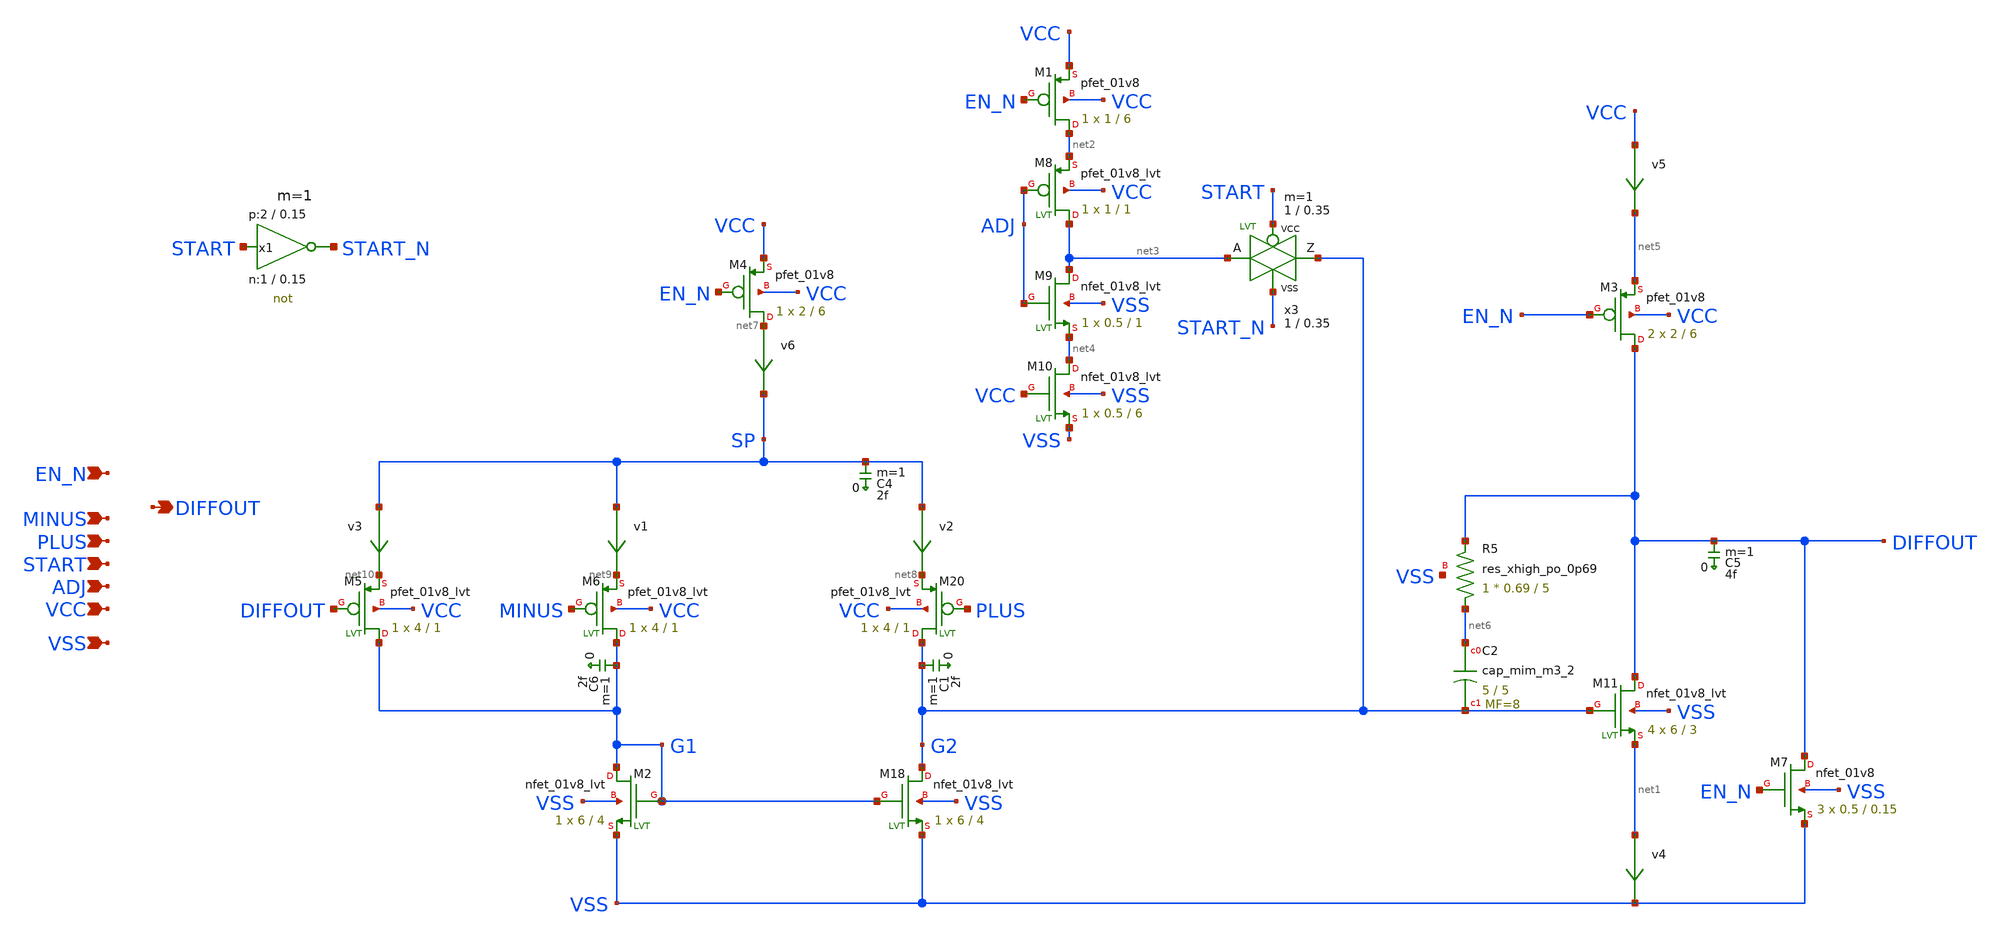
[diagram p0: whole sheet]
** sch_path: xyce/sky130A-xyce/libs.tech/xschem/sky130_tests/bandgap_opamp.sch
* Copyright 2020 Stefan Frederik Schippers
* Licensed under the Apache License, Version 2.0 (the "License");
* you may not use this file except in compliance with the License.
* You may obtain a copy of the License at
* https://www.apache.org/licenses/LICENSE-2.0
* Unless required by applicable law or agreed to in writing, software
* distributed under the License is distributed on an "AS IS" BASIS,
* WITHOUT WARRANTIES OR CONDITIONS OF ANY KIND, either express or implied.
* See the License for the specific language governing permissions and
* limitations under the License.
**.subckt bandgap_opamp PLUS MINUS EN_N VSS VCC DIFFOUT ADJ START
*.ipin PLUS
*.ipin MINUS
*.ipin EN_N
*.ipin VSS
*.ipin VCC
*.opin DIFFOUT
*.ipin ADJ
*.ipin START
C6 G1 0 2f m=1
XM4 net7 EN_N VCC VCC sky130_fd_pr__pfet_01v8 L=6 W=2 nf=1 ad='W * 0.29' as='W * 0.29' pd='W + 2 * 0.29'
+ ps='W + 2 * 0.29' nrd=0 nrs=0 sa=0 sb=0 sd=0 mult=1 m=1
XM18 G2 G1 VSS VSS sky130_fd_pr__nfet_01v8_lvt L=4 W=6 nf=1 ad='W * 0.29' as='W * 0.29' pd='2*(W + 0.29)'
+ ps='2*(W + 0.29)' nrd=0 nrs=0 sa=0 sb=0 sd=0 mult=1 m=1
XM2 G1 G1 VSS VSS sky130_fd_pr__nfet_01v8_lvt L=4 W=6 nf=1 ad='W * 0.29' as='W * 0.29' pd='2*(W + 0.29)'
+ ps='2*(W + 0.29)' nrd=0 nrs=0 sa=0 sb=0 sd=0 mult=1 m=1
XM20 G2 PLUS net8 VCC sky130_fd_pr__pfet_01v8_lvt L=1 W=4 nf=1 ad='W * 0.29' as='W * 0.29' pd='2*(W + 0.29)'
+ ps='2*(W + 0.29)' nrd=0 nrs=0 sa=0 sb=0 sd=0 mult=1 m=1
XM6 G1 MINUS net9 VCC sky130_fd_pr__pfet_01v8_lvt L=1 W=4 nf=1 ad='W * 0.29' as='W * 0.29' pd='2*(W + 0.29)'
+ ps='2*(W + 0.29)' nrd=0 nrs=0 sa=0 sb=0 sd=0 mult=1 m=1
v1 SP net9 0
.save i(v1)
C4 SP 0 2f m=1
C1 G2 0 2f m=1
C5 DIFFOUT 0 4f m=1
XM11 DIFFOUT G2 net1 VSS sky130_fd_pr__nfet_01v8_lvt L=3 W=6 nf=1 ad='W * 0.29' as='W * 0.29' pd='2*(W + 0.29)'
+ ps='2*(W + 0.29)' nrd=0 nrs=0 sa=0 sb=0 sd=0 mult=4 m=4
v2 SP net8 0
.save i(v2)
XM5 G1 DIFFOUT net10 VCC sky130_fd_pr__pfet_01v8_lvt L=1 W=4 nf=1 ad='W * 0.29' as='W * 0.29' pd='2*(W + 0.29)'
+ ps='2*(W + 0.29)' nrd=0 nrs=0 sa=0 sb=0 sd=0 mult=1 m=1
v3 SP net10 0
.save i(v3)
v4 net1 VSS 0
.save i(v4)
v5 VCC net5 0
.save i(v5)
v6 net7 SP 0
.save i(v6)
XM7 DIFFOUT EN_N VSS VSS sky130_fd_pr__nfet_01v8 L=0.15 W=0.5 nf=1 ad='W * 0.29' as='W * 0.29' pd='2*(W + 0.29)'
+ ps='2*(W + 0.29)' nrd=0 nrs=0 sa=0 sb=0 sd=0 mult=3 m=3
XM1 net2 EN_N VCC VCC sky130_fd_pr__pfet_01v8 L=6 W=1 nf=1 ad='W * 0.29' as='W * 0.29' pd='W + 2 * 0.29'
+ ps='W + 2 * 0.29' nrd=0 nrs=0 sa=0 sb=0 sd=0 mult=1 m=1
XM8 net3 ADJ net2 VCC sky130_fd_pr__pfet_01v8_lvt L=1 W=1 nf=1 ad='W * 0.29' as='W * 0.29' pd='W + 2 * 0.29'
+ ps='W + 2 * 0.29' nrd=0 nrs=0 sa=0 sb=0 sd=0 mult=1 m=1
XM9 net3 ADJ net4 VSS sky130_fd_pr__nfet_01v8_lvt L=1 W=0.5 nf=1 ad='W * 0.29' as='W * 0.29' pd='W + 2 * 0.29'
+ ps='W + 2 * 0.29' nrd=0 nrs=0 sa=0 sb=0 sd=0 mult=1 m=1
XM10 net4 VCC VSS VSS sky130_fd_pr__nfet_01v8_lvt L=6 W=0.5 nf=1 ad='W * 0.29' as='W * 0.29' pd='2*(W + 0.29)'
+ ps='2*(W + 0.29)' nrd=0 nrs=0 sa=0 sb=0 sd=0 mult=1 m=1
x1 START_N START VCC VSS not W_N=1 L_N=0.15 W_P=2 L_P=0.15 m=1
x3 G2 net3 START START_N VCC VSS passgate_nlvt W_N=1 L_N=0.35 W_P=1 L_P=0.35 m=1
XM3 DIFFOUT EN_N net5 VCC sky130_fd_pr__pfet_01v8 L=6 W=2 nf=1 ad='W * 0.29' as='W * 0.29' pd='W + 2 * 0.29'
+ ps='W + 2 * 0.29' nrd=0 nrs=0 sa=0 sb=0 sd=0 mult=2 m=2
XC2 net6 G2 sky130_fd_pr__cap_mim_m3_2 W=5 L=5 MF=8 m=8
XR5 net6 DIFFOUT VSS sky130_fd_pr__res_xhigh_po_0p69 W=0.69 L=5 mult=1 m=1
**** begin user architecture code

.include $::SKYWATER_MODELS/cells/nfet_01v8/sky130_fd_pr__nfet_01v8__tt.corner.spice
.include $::SKYWATER_MODELS/cells/nfet_01v8_lvt/sky130_fd_pr__nfet_01v8_lvt__tt.corner.spice
.include $::SKYWATER_MODELS/cells/pfet_01v8/sky130_fd_pr__pfet_01v8__tt.corner.spice
.include $::SKYWATER_MODELS/cells/nfet_03v3_nvt/sky130_fd_pr__nfet_03v3_nvt__tt.corner.spice
.include $::SKYWATER_MODELS/cells/nfet_05v0_nvt/sky130_fd_pr__nfet_05v0_nvt__tt.corner.spice
.include $::SKYWATER_MODELS/cells/esd_nfet_01v8/sky130_fd_pr__esd_nfet_01v8__tt.corner.spice
.include $::SKYWATER_MODELS/cells/pfet_01v8_lvt/sky130_fd_pr__pfet_01v8_lvt__tt.corner.spice
.include $::SKYWATER_MODELS/cells/pfet_01v8_hvt/sky130_fd_pr__pfet_01v8_hvt__tt.corner.spice
.include $::SKYWATER_MODELS/cells/esd_pfet_g5v0d10v5/sky130_fd_pr__esd_pfet_g5v0d10v5__tt.corner.spice
.include $::SKYWATER_MODELS/cells/pfet_g5v0d10v5/sky130_fd_pr__pfet_g5v0d10v5__tt.corner.spice
.include $::SKYWATER_MODELS/cells/pfet_g5v0d16v0/sky130_fd_pr__pfet_g5v0d16v0__tt.corner.spice
.include $::SKYWATER_MODELS/cells/nfet_g5v0d10v5/sky130_fd_pr__nfet_g5v0d10v5__tt.corner.spice
.include $::SKYWATER_MODELS/cells/nfet_g5v0d16v0/sky130_fd_pr__nfet_g5v0d16v0__tt_discrete.corner.spice
.include $::SKYWATER_MODELS/cells/esd_nfet_g5v0d10v5/sky130_fd_pr__esd_nfet_g5v0d10v5__tt.corner.spice
.include $::SKYWATER_MODELS/models/corners/tt/nonfet.spice
* Mismatch parameters
.include $::SKYWATER_MODELS/cells/nfet_01v8/sky130_fd_pr__nfet_01v8__mismatch.corner.spice
.include $::SKYWATER_MODELS/cells/pfet_01v8/sky130_fd_pr__pfet_01v8__mismatch.corner.spice
.include $::SKYWATER_MODELS/cells/nfet_01v8_lvt/sky130_fd_pr__nfet_01v8_lvt__mismatch.corner.spice
.include $::SKYWATER_MODELS/cells/pfet_01v8_lvt/sky130_fd_pr__pfet_01v8_lvt__mismatch.corner.spice
.include $::SKYWATER_MODELS/cells/pfet_01v8_hvt/sky130_fd_pr__pfet_01v8_hvt__mismatch.corner.spice
.include $::SKYWATER_MODELS/cells/nfet_g5v0d10v5/sky130_fd_pr__nfet_g5v0d10v5__mismatch.corner.spice
.include $::SKYWATER_MODELS/cells/pfet_g5v0d10v5/sky130_fd_pr__pfet_g5v0d10v5__mismatch.corner.spice
.include $::SKYWATER_MODELS/cells/nfet_05v0_nvt/sky130_fd_pr__nfet_05v0_nvt__mismatch.corner.spice
.include $::SKYWATER_MODELS/cells/nfet_03v3_nvt/sky130_fd_pr__nfet_03v3_nvt__mismatch.corner.spice
* Resistor$::SKYWATER_MODELS/Capacitor
.include $::SKYWATER_MODELS/models/r+c/res_typical__cap_typical.spice
.include $::SKYWATER_MODELS/models/r+c/res_typical__cap_typical__lin.spice
* Special cells
.include $::SKYWATER_MODELS/models/corners/tt/specialized_cells.spice
* All models
.include $::SKYWATER_MODELS/models/all.spice
* Corner
.include $::SKYWATER_MODELS/models/corners/tt/rf.spice

**** end user architecture code
**.ends

* expanding   symbol:  sky130_tests/not.sym # of pins=2
** sym_path: xyce/sky130A-xyce/libs.tech/xschem/sky130_tests/not.sym
** sch_path: xyce/sky130A-xyce/libs.tech/xschem/sky130_tests/not.sch
.subckt not y a VCCPIN VSSPIN     W_N=1 L_N=0.15 W_P=2 L_P=0.15
*.opin y
*.ipin a
XM1 y a VSSPIN VSSPIN sky130_fd_pr__nfet_01v8 L=L_N W=W_N nf=1 ad='int((nf+1)/2) * W/nf * 0.29' as='int((nf+2)/2) * W/nf * 0.29'
+ pd='2*int((nf+1)/2) * (W/nf + 0.29)' ps='2*int((nf+2)/2) * (W/nf + 0.29)' nrd='0.29 / W' nrs='0.29 / W'
+ sa=0 sb=0 sd=0 mult=1 m=1
XM2 y a VCCPIN VCCPIN sky130_fd_pr__pfet_01v8 L=L_P W=W_P nf=1 ad='int((nf+1)/2) * W/nf * 0.29' as='int((nf+2)/2) * W/nf * 0.29'
+ pd='2*int((nf+1)/2) * (W/nf + 0.29)' ps='2*int((nf+2)/2) * (W/nf + 0.29)' nrd='0.29 / W' nrs='0.29 / W'
+ sa=0 sb=0 sd=0 mult=1 m=1
.ends


* expanding   symbol:  sky130_tests/passgate_nlvt.sym # of pins=4
** sym_path: xyce/sky130A-xyce/libs.tech/xschem/sky130_tests/passgate_nlvt.sym
** sch_path: xyce/sky130A-xyce/libs.tech/xschem/sky130_tests/passgate_nlvt.sch
.subckt passgate_nlvt Z A GP GN VCCBPIN VSSBPIN  W_N=1 L_N=0.35 W_P=1 L_P=0.35
*.iopin A
*.iopin Z
*.ipin GP
*.ipin GN
XM1 Z GN A VSSBPIN sky130_fd_pr__nfet_01v8_lvt L=L_N W=W_N nf=1 ad='int((nf+1)/2) * W/nf * 0.29' as='int((nf+2)/2) * W/nf * 0.29'
+ pd='2*int((nf+1)/2) * (W/nf + 0.29)' ps='2*int((nf+2)/2) * (W/nf + 0.29)' nrd='0.29 / W' nrs='0.29 / W'
+ sa=0 sb=0 sd=0 mult=1 m=1
XM2 Z GP A VCCBPIN sky130_fd_pr__pfet_01v8_lvt L=L_P W=W_P nf=1 ad='int((nf+1)/2) * W/nf * 0.29' as='int((nf+2)/2) * W/nf * 0.29'
+ pd='2*int((nf+1)/2) * (W/nf + 0.29)' ps='2*int((nf+2)/2) * (W/nf + 0.29)' nrd='0.29 / W' nrs='0.29 / W'
+ sa=0 sb=0 sd=0 mult=1 m=1
.ends

**** begin user architecture code

* .option SCALE=1e-6
.option method=gear seed=12

* this experimental option enables mos model bin
* selection based on W/NF instead of W
.option wnflag=1

.param VCC=1.6
* .param VCCGAUSS=agauss(1.8, 0.05, 1)
* .param VCC=VCCGAUSS
.param VDL=0.7
.param ABSVAR=0.0
.temp 25

** to generate following file:
** copy .../xschem_sky130/sky130_tests/stimuli.test_comparator to simulation directory
** then do 'Simulation->Utile Stimuli Editor (GUI)' and press 'Translate'
.include "stimuli_bandgap_opamp.cir"

** variation marameters:
* .param sky130_fd_pr__nfet_01v8_lvt__vth0_slope_spectre='agauss(0, ABSVAR, 3)/sky130_fd_pr__nfet_01v8_lvt__vth0_slope'
* .param sky130_fd_pr__pfet_01v8_lvt__vth0_slope_spectre='agauss(0, ABSVAR, 3)/sky130_fd_pr__pfet_01v8_lvt__vth0_slope'

* .tran 0.1n 900n uic

.control
  let run=1
  dowhile run <= 1
    if run > 1
      reset
      set appendwrite
    end
    save all
    * save saout cal i(vvcc) en plus minus
    tran 1n 10000n uic
    plot diffout
    plot plus minus
    write bandgap_opamp.raw
    let run = run + 1
  end
.endc


**** end user architecture code
.end
